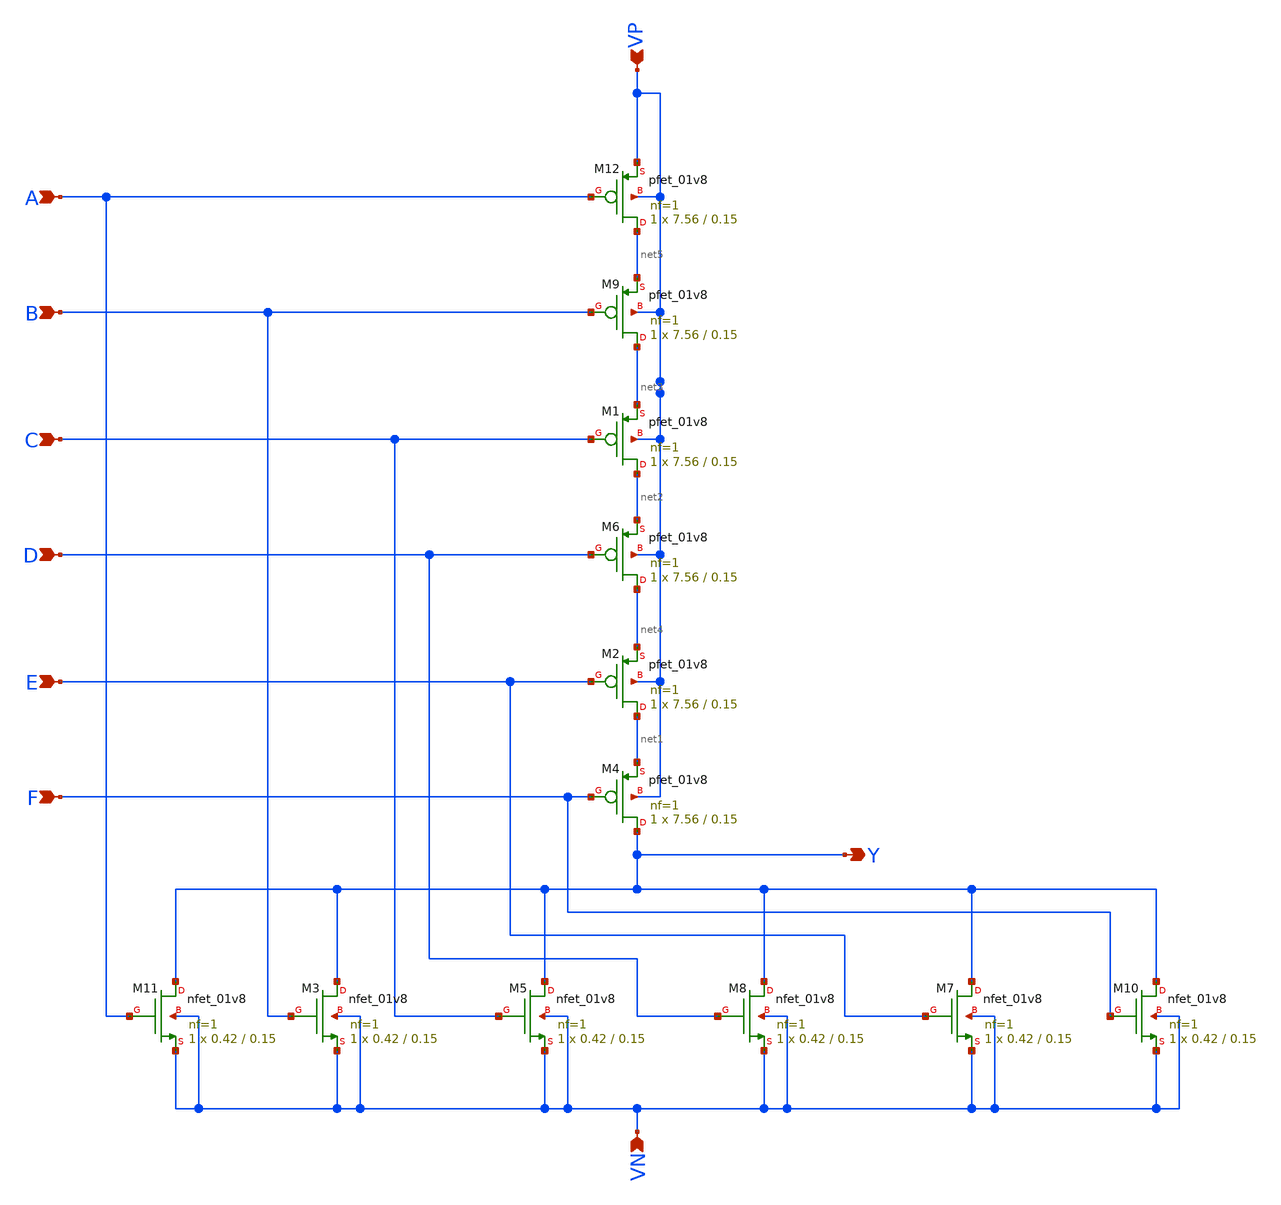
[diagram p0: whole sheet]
** sch_path: component/NOR6/nor6.sch
**.subckt nor6 Y D E B C A F VP VN
*.opin Y
*.ipin D
*.ipin E
*.ipin B
*.ipin C
*.ipin A
*.ipin F
*.ipin VP
*.ipin VN
XM5 Y C VN VN sky130_fd_pr__nfet_01v8 L=0.15 W=0.42 nf=1 ad='int((nf+1)/2) * W/nf * 0.29' as='int((nf+2)/2) * W/nf * 0.29'
+ pd='2*int((nf+1)/2) * (W/nf + 0.29)' ps='2*int((nf+2)/2) * (W/nf + 0.29)' nrd='0.29 / W' nrs='0.29 / W'
+ sa=0 sb=0 sd=0 mult=1 m=1
XM3 Y B VN VN sky130_fd_pr__nfet_01v8 L=0.15 W=0.42 nf=1 ad='int((nf+1)/2) * W/nf * 0.29' as='int((nf+2)/2) * W/nf * 0.29'
+ pd='2*int((nf+1)/2) * (W/nf + 0.29)' ps='2*int((nf+2)/2) * (W/nf + 0.29)' nrd='0.29 / W' nrs='0.29 / W'
+ sa=0 sb=0 sd=0 mult=1 m=1
XM2 net1 E net4 VP sky130_fd_pr__pfet_01v8 L=0.15 W=7.56 nf=1 ad='int((nf+1)/2) * W/nf * 0.29' as='int((nf+2)/2) * W/nf * 0.29'
+ pd='2*int((nf+1)/2) * (W/nf + 0.29)' ps='2*int((nf+2)/2) * (W/nf + 0.29)' nrd='0.29 / W' nrs='0.29 / W'
+ sa=0 sb=0 sd=0 mult=1 m=1
XM4 Y F net1 VP sky130_fd_pr__pfet_01v8 L=0.15 W=7.56 nf=1 ad='int((nf+1)/2) * W/nf * 0.29' as='int((nf+2)/2) * W/nf * 0.29'
+ pd='2*int((nf+1)/2) * (W/nf + 0.29)' ps='2*int((nf+2)/2) * (W/nf + 0.29)' nrd='0.29 / W' nrs='0.29 / W'
+ sa=0 sb=0 sd=0 mult=1 m=1
XM1 net2 C net3 VP sky130_fd_pr__pfet_01v8 L=0.15 W=7.56 nf=1 ad='int((nf+1)/2) * W/nf * 0.29' as='int((nf+2)/2) * W/nf * 0.29'
+ pd='2*int((nf+1)/2) * (W/nf + 0.29)' ps='2*int((nf+2)/2) * (W/nf + 0.29)' nrd='0.29 / W' nrs='0.29 / W'
+ sa=0 sb=0 sd=0 mult=1 m=1
XM6 net4 D net2 VP sky130_fd_pr__pfet_01v8 L=0.15 W=7.56 nf=1 ad='int((nf+1)/2) * W/nf * 0.29' as='int((nf+2)/2) * W/nf * 0.29'
+ pd='2*int((nf+1)/2) * (W/nf + 0.29)' ps='2*int((nf+2)/2) * (W/nf + 0.29)' nrd='0.29 / W' nrs='0.29 / W'
+ sa=0 sb=0 sd=0 mult=1 m=1
XM7 Y E VN VN sky130_fd_pr__nfet_01v8 L=0.15 W=0.42 nf=1 ad='int((nf+1)/2) * W/nf * 0.29' as='int((nf+2)/2) * W/nf * 0.29'
+ pd='2*int((nf+1)/2) * (W/nf + 0.29)' ps='2*int((nf+2)/2) * (W/nf + 0.29)' nrd='0.29 / W' nrs='0.29 / W'
+ sa=0 sb=0 sd=0 mult=1 m=1
XM8 Y D VN VN sky130_fd_pr__nfet_01v8 L=0.15 W=0.42 nf=1 ad='int((nf+1)/2) * W/nf * 0.29' as='int((nf+2)/2) * W/nf * 0.29'
+ pd='2*int((nf+1)/2) * (W/nf + 0.29)' ps='2*int((nf+2)/2) * (W/nf + 0.29)' nrd='0.29 / W' nrs='0.29 / W'
+ sa=0 sb=0 sd=0 mult=1 m=1
XM9 net3 B net5 VP sky130_fd_pr__pfet_01v8 L=0.15 W=7.56 nf=1 ad='int((nf+1)/2) * W/nf * 0.29' as='int((nf+2)/2) * W/nf * 0.29'
+ pd='2*int((nf+1)/2) * (W/nf + 0.29)' ps='2*int((nf+2)/2) * (W/nf + 0.29)' nrd='0.29 / W' nrs='0.29 / W'
+ sa=0 sb=0 sd=0 mult=1 m=1
XM10 Y F VN VN sky130_fd_pr__nfet_01v8 L=0.15 W=0.42 nf=1 ad='int((nf+1)/2) * W/nf * 0.29' as='int((nf+2)/2) * W/nf * 0.29'
+ pd='2*int((nf+1)/2) * (W/nf + 0.29)' ps='2*int((nf+2)/2) * (W/nf + 0.29)' nrd='0.29 / W' nrs='0.29 / W'
+ sa=0 sb=0 sd=0 mult=1 m=1
XM11 Y A VN VN sky130_fd_pr__nfet_01v8 L=0.15 W=0.42 nf=1 ad='int((nf+1)/2) * W/nf * 0.29' as='int((nf+2)/2) * W/nf * 0.29'
+ pd='2*int((nf+1)/2) * (W/nf + 0.29)' ps='2*int((nf+2)/2) * (W/nf + 0.29)' nrd='0.29 / W' nrs='0.29 / W'
+ sa=0 sb=0 sd=0 mult=1 m=1
XM12 net5 A VP VP sky130_fd_pr__pfet_01v8 L=0.15 W=7.56 nf=1 ad='int((nf+1)/2) * W/nf * 0.29' as='int((nf+2)/2) * W/nf * 0.29'
+ pd='2*int((nf+1)/2) * (W/nf + 0.29)' ps='2*int((nf+2)/2) * (W/nf + 0.29)' nrd='0.29 / W' nrs='0.29 / W'
+ sa=0 sb=0 sd=0 mult=1 m=1
**.ends
.end
